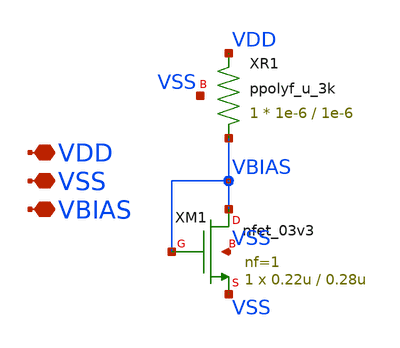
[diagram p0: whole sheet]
** sch_path: designs/libs/core_current-mirror/nbias-gen/nbias-gen.sch
**.subckt nbias-gen VDD VSS VBIAS
*.iopin VDD
*.iopin VSS
*.iopin VBIAS
XM1 VBIAS VBIAS VSS VSS nfet_03v3 L=0.28u W=0.22u nf=1 ad='int((nf+1)/2) * W/nf * 0.18u' as='int((nf+2)/2) * W/nf * 0.18u'
+ pd='2*int((nf+1)/2) * (W/nf + 0.18u)' ps='2*int((nf+2)/2) * (W/nf + 0.18u)' nrd='0.18u / W' nrs='0.18u / W'
+ sa=0 sb=0 sd=0 m=1
XR1 VBIAS VDD VSS ppolyf_u_3k r_width=1e-6 r_length=1e-6 m=1
**.ends
.end
